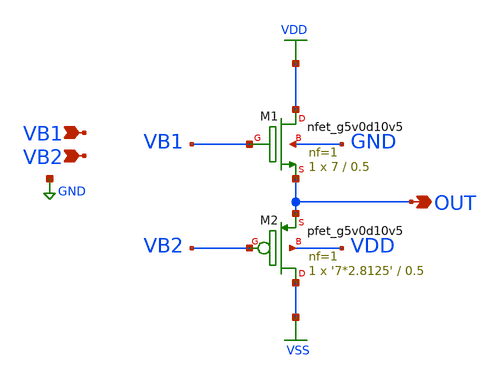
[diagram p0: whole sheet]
** sch_path: schem/voltage-reg.sch
**.subckt voltage-reg OUT VB2 VB1
*.opin OUT
*.ipin VB2
*.ipin VB1
XM1 VDD VB1 OUT GND sky130_fd_pr__nfet_g5v0d10v5 L=0.5 W=7 nf=1 ad='int((nf+1)/2) * W/nf * 0.29' as='int((nf+2)/2) * W/nf * 0.29'
+ pd='2*int((nf+1)/2) * (W/nf + 0.29)' ps='2*int((nf+2)/2) * (W/nf + 0.29)' nrd='0.29 / W' nrs='0.29 / W'
+ sa=0 sb=0 sd=0 mult=1 m=1
XM2 VSS VB2 OUT VDD sky130_fd_pr__pfet_g5v0d10v5 L=0.5 W='7*2.8125' nf=1 ad='int((nf+1)/2) * W/nf * 0.29'
+ as='int((nf+2)/2) * W/nf * 0.29' pd='2*int((nf+1)/2) * (W/nf + 0.29)' ps='2*int((nf+2)/2) * (W/nf + 0.29)'
+ nrd='0.29 / W' nrs='0.29 / W' sa=0 sb=0 sd=0 mult=1 m=1
**.ends
.GLOBAL VDD
.GLOBAL VSS
.GLOBAL GND
.end
